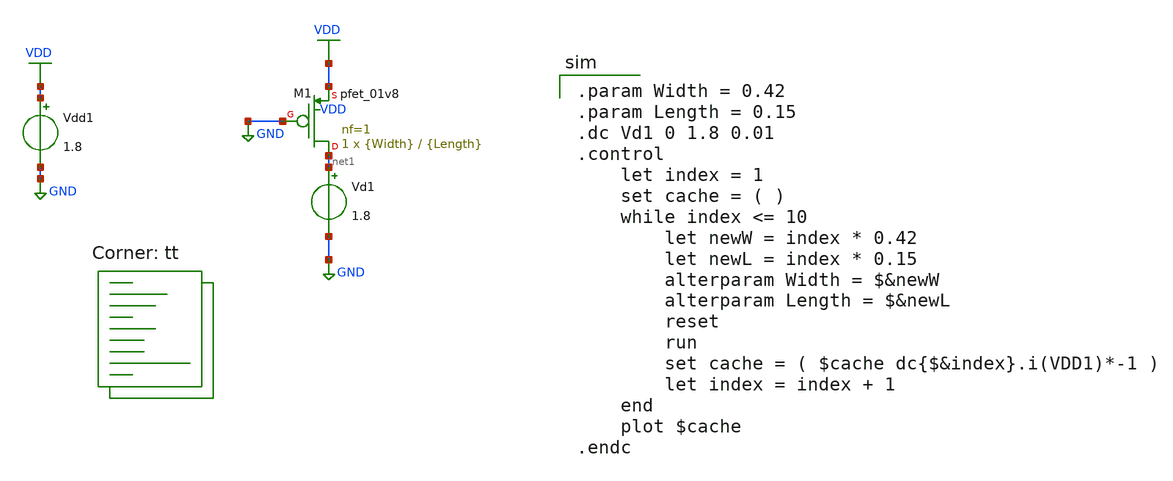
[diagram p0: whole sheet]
** sch_path: tutorial-1/source/q2c.sch
**.subckt q2c
Vdd1 VDD GND 1.8
XM1 net1 GND VDD VDD sky130_fd_pr__pfet_01v8 L={Length} W={Width} nf=1 ad='int((nf+1)/2) * W/nf * 0.29'
+ as='int((nf+2)/2) * W/nf * 0.29' pd='2*int((nf+1)/2) * (W/nf + 0.29)' ps='2*int((nf+2)/2) * (W/nf + 0.29)'
+ nrd='0.29 / W' nrs='0.29 / W' sa=0 sb=0 sd=0 mult=1 m=1
Vd1 net1 GND 1.8
**** begin user architecture code
.lib $::SKYWATER_MODELS/sky130.lib.spice tt

.param Width = 0.42
.param Length = 0.15
.dc Vd1 0 1.8 0.01
.control
    let index = 1
    set cache = ( )
    while index <= 10
        let newW = index * 0.42
        let newL = index * 0.15
        alterparam Width = $&newW
        alterparam Length = $&newL
        reset
        run
        set cache = ( $cache dc{$&index}.i(VDD1)*-1 )
        let index = index + 1
    end
    plot $cache
.endc

**** end user architecture code
**.ends
.GLOBAL VDD
.GLOBAL GND
.end
